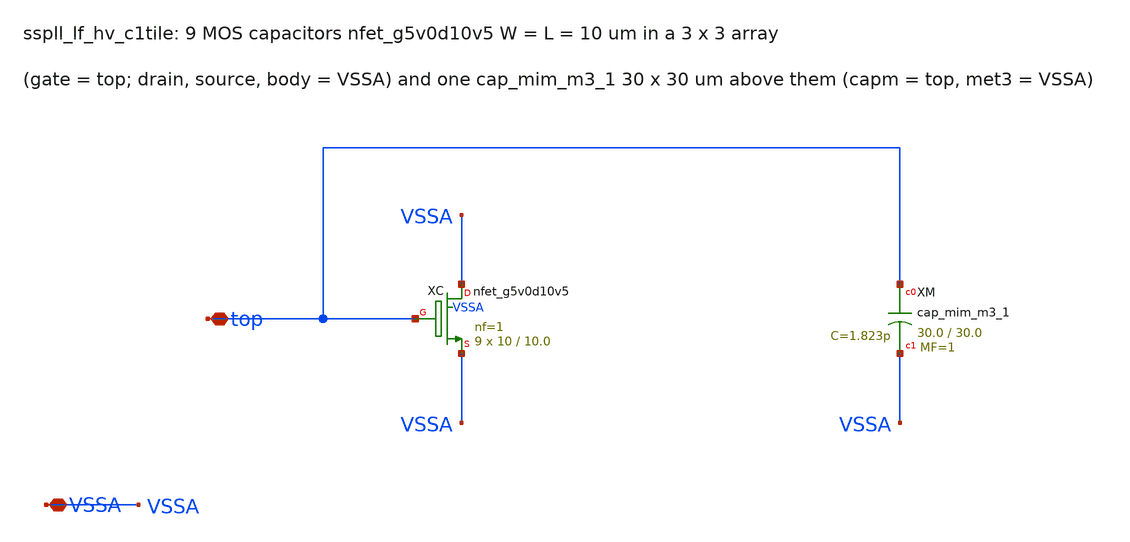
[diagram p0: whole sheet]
** sch_path: xschem/lf_hv/sspll_lf_hv_c1tile.sch
**.subckt sspll_lf_hv_c1tile top VSSA
*.iopin top
*.iopin VSSA
XXC VSSA top VSSA VSSA sky130_fd_pr__nfet_g5v0d10v5 L=10.0 W=10 nf=1 ad='int((nf+1)/2) * W/nf * 0.29'
+ as='int((nf+2)/2) * W/nf * 0.29' pd='2*int((nf+1)/2) * (W/nf + 0.29)' ps='2*int((nf+2)/2) * (W/nf + 0.29)'
+ nrd='0.29 / W' nrs='0.29 / W' sa=0 sb=0 sd=0 mult=9 m=9
XXM top VSSA sky130_fd_pr__cap_mim_m3_1 W=30.0 L=30.0 MF=1 m=1
**.ends
.end
